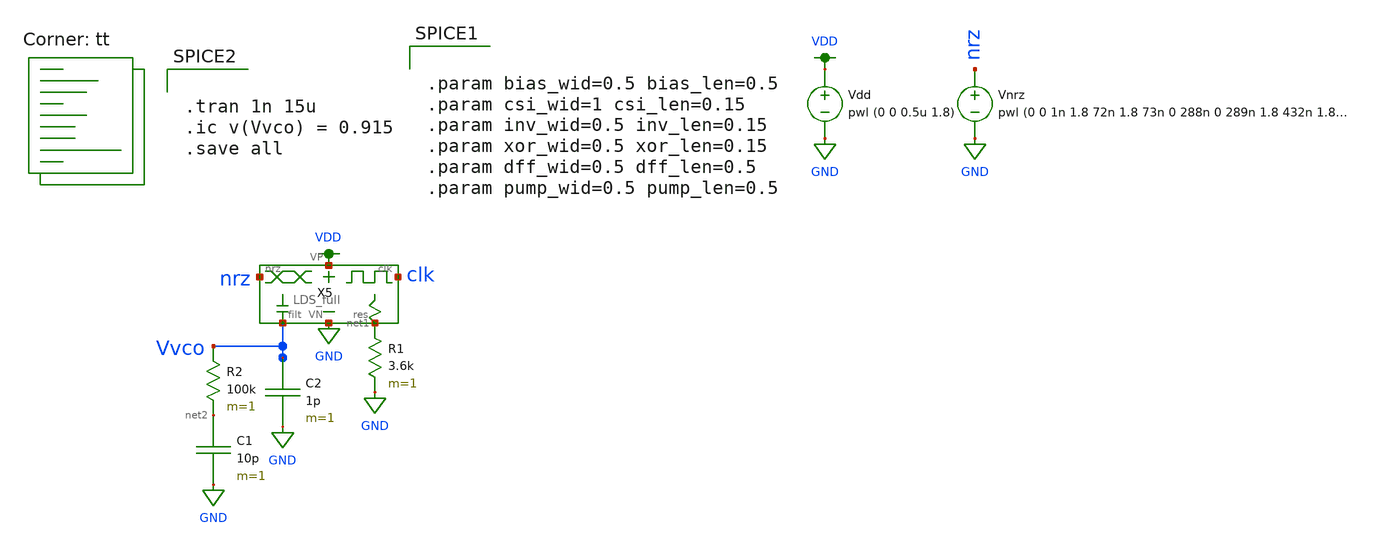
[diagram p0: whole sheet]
** sch_path: LDS/test_full_no_passive.sch
**.subckt test_full_no_passive
Vdd VDD GND pwl (0 0 0.5u 1.8)
Vnrz nrz GND pwl (0 0 1n 1.8 72n 1.8 73n 0 288n 0 289n 1.8 432n 1.8 433n 0 504n 0) R=0 td=1u
R1 net1 GND 3.6k m=1
R2 Vvco net2 100k m=1
C1 net2 GND 10p m=1
C2 Vvco GND 1p m=1
X5 VDD GND Vvco nrz net1 clk LDS_full
**** begin user architecture code
.lib $::SKYWATER_MODELS/sky130.lib.spice tt


.tran 1n 15u
.ic v(Vvco) = 0.915
.save all




.param bias_wid=0.5 bias_len=0.5
.param csi_wid=1 csi_len=0.15
.param inv_wid=0.5 inv_len=0.15
.param xor_wid=0.5 xor_len=0.15
.param dff_wid=0.5 dff_len=0.5
.param pump_wid=0.5 pump_len=0.5


**** end user architecture code
**.ends
.GLOBAL VDD
.GLOBAL GND
.end
